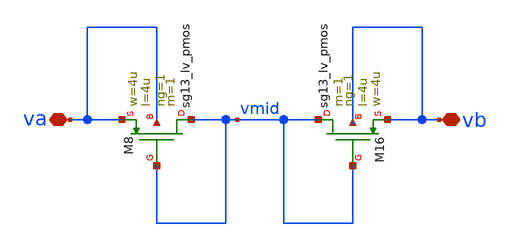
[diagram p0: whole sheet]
** sch_path: v2_feature_extr_withf/pseudo_res.sch
**.subckt pseudo_res va vb
*.iopin va
*.iopin vb
XM8 vmid vmid va va sg13_lv_pmos w=4u l=4u ng=1 m=1 mm_ok=1
XM16 vmid vmid vb vb sg13_lv_pmos w=4u l=4u ng=1 m=1 mm_ok=1
**.ends
.end
